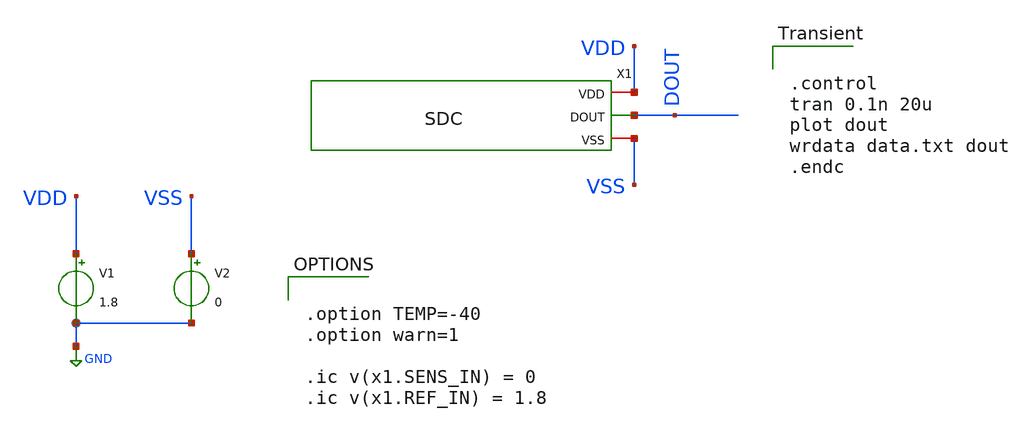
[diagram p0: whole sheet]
** sch_path: modules/SDC/test/test_SDCtsens_RINtsweep_9p1_ROrangeext.sch
**.subckt test_SDCtsens_RINtsweep_9p1_ROrangeext
V1 VDD GND 1.8
V2 VSS GND 0
X1 VDD DOUT VSS SDC
**** begin user architecture code

** opencircuitdesign pdks install
.lib $env(PDK_ROOT)/$env(PDK)/libs.tech/ngspice/sky130.lib.spice.tt.red tt
*.lib $env(PDK_ROOT)/$env(PDK)/libs.tech/combined/sky130.lib.spice tt



.control
tran 0.1n 20u
plot dout
wrdata data.txt dout
.endc



.option TEMP=-40
.option warn=1

.ic v(x1.SENS_IN) = 0
.ic v(x1.REF_IN) = 1.8


**** end user architecture code
**.ends
.GLOBAL GND
.end
